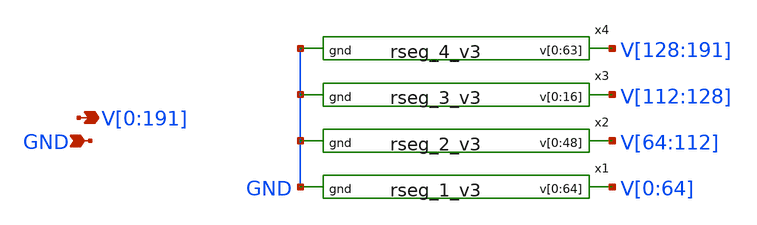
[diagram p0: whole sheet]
** sch_path: xschem/rstring_v3.sch
**.subckt rstring_v3
*+ V[0],V[1],V[2],V[3],V[4],V[5],V[6],V[7],V[8],V[9],V[10],V[11],V[12],V[13],V[14],V[15],V[16],V[17],V[18],V[19],V[20],V[21],V[22],V[23],V[24],V[25],V[26],V[27],V[28],V[29],V[30],V[31],V[32],V[33],V[34],V[35],V[36],V[37],V[38],V[39],V[40],V[41],V[42],V[43],V[44],V[45],V[46],V[47],V[48],V[49],V[50],V[51],V[52],V[53],V[54],V[55],V[56],V[57],V[58],V[59],V[60],V[61],V[62],V[63],V[64],V[65],V[66],V[67],V[68],V[69],V[70],V[71],V[72],V[73],V[74],V[75],V[76],V[77],V[78],V[79],V[80],V[81],V[82],V[83],V[84],V[85],V[86],V[87],V[88],V[89],V[90],V[91],V[92],V[93],V[94],V[95],V[96],V[97],V[98],V[99],V[100],V[101],V[102],V[103],V[104],V[105],V[106],V[107],V[108],V[109],V[110],V[111],V[112],V[113],V[114],V[115],V[116],V[117],V[118],V[119],V[120],V[121],V[122],V[123],V[124],V[125],V[126],V[127],V[128],V[129],V[130],V[131],V[132],V[133],V[134],V[135],V[136],V[137],V[138],V[139],V[140],V[141],V[142],V[143],V[144],V[145],V[146],V[147],V[148],V[149],V[150],V[151],V[152],V[153],V[154],V[155],V[156],V[157],V[158],V[159],V[160],V[161],V[162],V[163],V[164],V[165],V[166],V[167],V[168],V[169],V[170],V[171],V[172],V[173],V[174],V[175],V[176],V[177],V[178],V[179],V[180],V[181],V[182],V[183],V[184],V[185],V[186],V[187],V[188],V[189],V[190],V[191] GND
*.opin
*+ V[0],V[1],V[2],V[3],V[4],V[5],V[6],V[7],V[8],V[9],V[10],V[11],V[12],V[13],V[14],V[15],V[16],V[17],V[18],V[19],V[20],V[21],V[22],V[23],V[24],V[25],V[26],V[27],V[28],V[29],V[30],V[31],V[32],V[33],V[34],V[35],V[36],V[37],V[38],V[39],V[40],V[41],V[42],V[43],V[44],V[45],V[46],V[47],V[48],V[49],V[50],V[51],V[52],V[53],V[54],V[55],V[56],V[57],V[58],V[59],V[60],V[61],V[62],V[63],V[64],V[65],V[66],V[67],V[68],V[69],V[70],V[71],V[72],V[73],V[74],V[75],V[76],V[77],V[78],V[79],V[80],V[81],V[82],V[83],V[84],V[85],V[86],V[87],V[88],V[89],V[90],V[91],V[92],V[93],V[94],V[95],V[96],V[97],V[98],V[99],V[100],V[101],V[102],V[103],V[104],V[105],V[106],V[107],V[108],V[109],V[110],V[111],V[112],V[113],V[114],V[115],V[116],V[117],V[118],V[119],V[120],V[121],V[122],V[123],V[124],V[125],V[126],V[127],V[128],V[129],V[130],V[131],V[132],V[133],V[134],V[135],V[136],V[137],V[138],V[139],V[140],V[141],V[142],V[143],V[144],V[145],V[146],V[147],V[148],V[149],V[150],V[151],V[152],V[153],V[154],V[155],V[156],V[157],V[158],V[159],V[160],V[161],V[162],V[163],V[164],V[165],V[166],V[167],V[168],V[169],V[170],V[171],V[172],V[173],V[174],V[175],V[176],V[177],V[178],V[179],V[180],V[181],V[182],V[183],V[184],V[185],V[186],V[187],V[188],V[189],V[190],V[191]
*.ipin GND
x1 V[0] V[1] V[2] V[3] V[4] V[5] V[6] V[7] V[8] V[9] V[10] V[11] V[12] V[13] V[14] V[15] V[16] V[17]
+ V[18] V[19] V[20] V[21] V[22] V[23] V[24] V[25] V[26] V[27] V[28] V[29] V[30] V[31] V[32] V[33] V[34]
+ V[35] V[36] V[37] V[38] V[39] V[40] V[41] V[42] V[43] V[44] V[45] V[46] V[47] V[48] V[49] V[50] V[51]
+ V[52] V[53] V[54] V[55] V[56] V[57] V[58] V[59] V[60] V[61] V[62] V[63] V[64] GND rseg_1_v3
x2 V[64] V[65] V[66] V[67] V[68] V[69] V[70] V[71] V[72] V[73] V[74] V[75] V[76] V[77] V[78] V[79]
+ V[80] V[81] V[82] V[83] V[84] V[85] V[86] V[87] V[88] V[89] V[90] V[91] V[92] V[93] V[94] V[95] V[96]
+ V[97] V[98] V[99] V[100] V[101] V[102] V[103] V[104] V[105] V[106] V[107] V[108] V[109] V[110] V[111]
+ V[112] GND rseg_2_v3
x3 V[112] V[113] V[114] V[115] V[116] V[117] V[118] V[119] V[120] V[121] V[122] V[123] V[124] V[125]
+ V[126] V[127] V[128] GND rseg_3_v3
x4 V[128] V[129] V[130] V[131] V[132] V[133] V[134] V[135] V[136] V[137] V[138] V[139] V[140] V[141]
+ V[142] V[143] V[144] V[145] V[146] V[147] V[148] V[149] V[150] V[151] V[152] V[153] V[154] V[155] V[156]
+ V[157] V[158] V[159] V[160] V[161] V[162] V[163] V[164] V[165] V[166] V[167] V[168] V[169] V[170] V[171]
+ V[172] V[173] V[174] V[175] V[176] V[177] V[178] V[179] V[180] V[181] V[182] V[183] V[184] V[185] V[186]
+ V[187] V[188] V[189] V[190] V[191] GND rseg_4_v3
**.ends
.end
